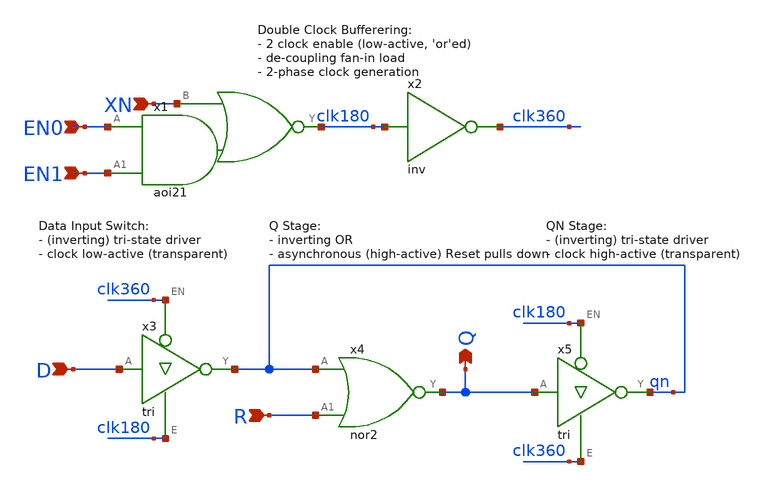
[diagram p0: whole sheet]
** sch_path: Sources/crafted/LATEERN.sch
**.subckt LATEERN XN D Q EN0 EN1 R
*.ipin XN
*.ipin D
*.opin Q
*.ipin EN0
*.ipin EN1
*.ipin R
x2 clk180 clk360 VDD GND inv Wmin=1.5u Lmin=1u g=2 m=1
x3 D clk360 clk180 qn VDD GND tri Wmin=1.5u Lmin=1u g=2 m=1
x5 Q clk180 clk360 qn VDD GND tri Wmin=1.5u Lmin=1u g=2 m=1
x1 EN0 EN1 clk180 XN VDD GND aoi21 Wmin=1.5u Lmin=1u g=2 m=1
x4 Q qn R VDD GND nor2 Wmin=1.5u Lmin=1u g=2 m=1
**.ends
.end
